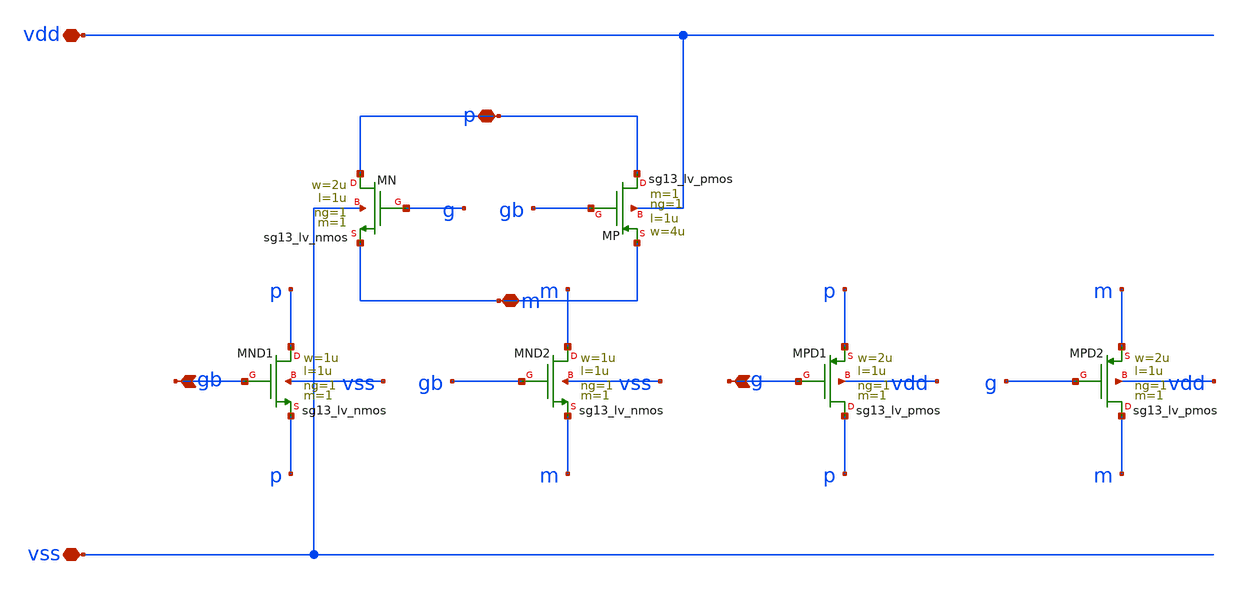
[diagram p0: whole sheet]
** sch_path: ip/dsm2_core/schematic/sw_tgate.sch
**.subckt sw_tgate vdd vss p m gb g
*.iopin vdd
*.iopin vss
*.iopin p
*.iopin m
*.ipin gb
*.ipin g
XMN p g m vss sg13_lv_nmos w=2u l=1u ng=1 m=1 mm_ok=1
XMP p gb m vdd sg13_lv_pmos w=4u l=1u ng=1 m=1 mm_ok=1
XMND1 p gb p vss sg13_lv_nmos w=1u l=1u ng=1 m=1 mm_ok=1
XMND2 m gb m vss sg13_lv_nmos w=1u l=1u ng=1 m=1 mm_ok=1
XMPD1 p g p vdd sg13_lv_pmos w=2u l=1u ng=1 m=1 mm_ok=1
XMPD2 m g m vdd sg13_lv_pmos w=2u l=1u ng=1 m=1 mm_ok=1
**.ends
.end
